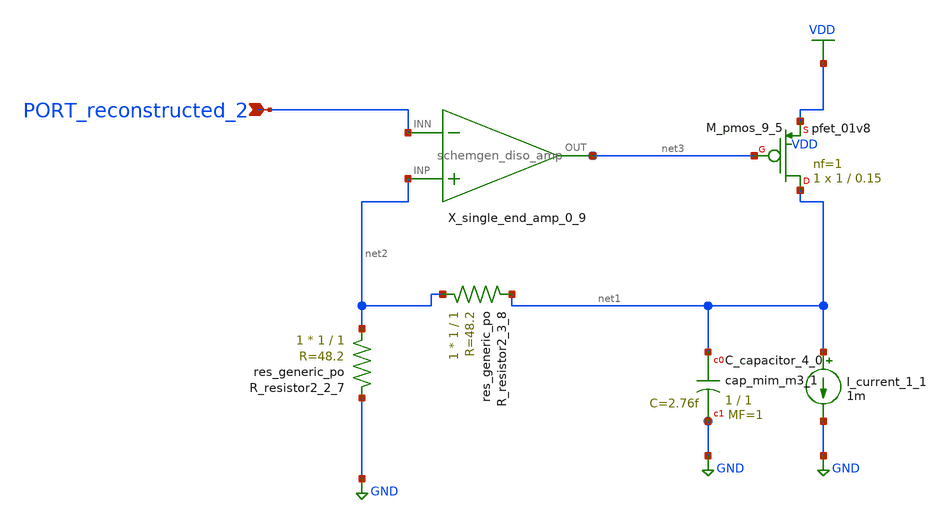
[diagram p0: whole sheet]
** sch_path: schematics/Image2Net/082.sch
**.subckt 082 PORT_reconstructed_2
*.ipin PORT_reconstructed_2
XC_capacitor_4_0 net1 GND sky130_fd_pr__cap_mim_m3_1 W=1 L=1 MF=1 m=1
I_current_1_1 net1 GND 1m
XM_pmos_9_5 net1 net3 VDD VDD sky130_fd_pr__pfet_01v8 L=0.15 W=1 nf=1 ad='int((1 + 1)/2) * 1 / 1 * 0.29'
+ as='int((1 + 2)/2) * 1 / 1 * 0.29' pd='2*int((1 + 1)/2) * (1 / 1 + 0.29)' ps='2*int((1 + 2)/2) * (1 / 1 + 0.29)'
+ nrd='0.29 / 1 ' nrs='0.29 / 1 ' sa=0 sb=0 sd=0 mult=1 m=1
XR_resistor2_2_7 net2 GND sky130_fd_pr__res_generic_po W=1 L=1 m=1
XR_resistor2_3_8 net2 net1 sky130_fd_pr__res_generic_po W=1 L=1 m=1
X_single_end_amp_0_9 net2 PORT_reconstructed_2 net3 schemgen_diso_amp
**.ends

* expanding   symbol:  schemgen_diso_amp.sym # of pins=3
** sym_path: symbols/schemgen_diso_amp.sym
.subckt schemgen_diso_amp INP INN OUT
* SchemGen ideal op-amp: Vout = 1e5 * (V(INP) - V(INN))
E1 OUT 0 INP INN 1e5
.ends schemgen_diso_amp
.GLOBAL GND
.GLOBAL VDD
.end
